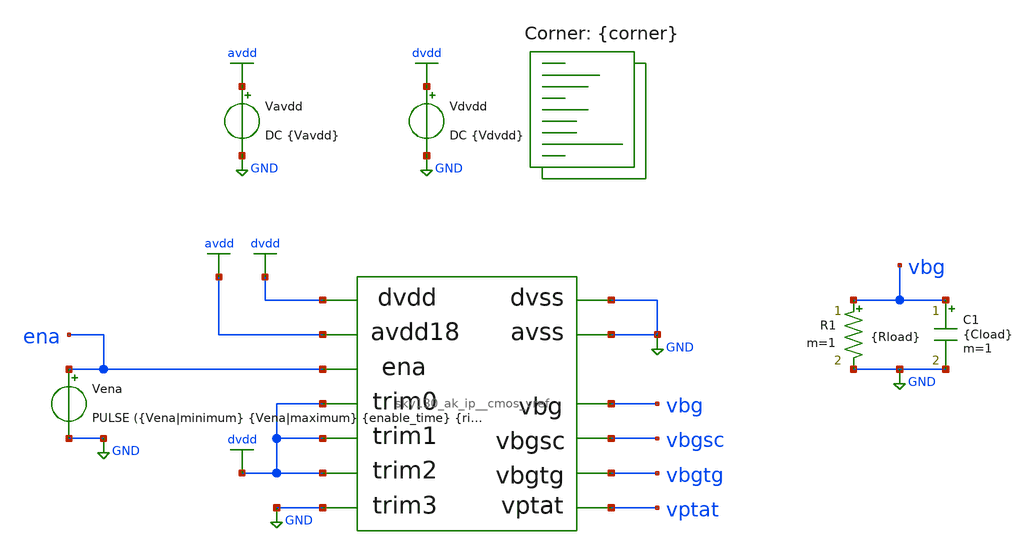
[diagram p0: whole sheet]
** sch_path: cace/tb_startup.sch
**.subckt tb_startup
Vavdd avdd GND DC {Vavdd}
X1 avdd GND dvdd vbg vptat dvdd dvdd GND dvdd GND ena vbgsc vbgtg sky130_ak_ip__cmos_vref
Vdvdd dvdd GND DC {Vdvdd}
C1 vbg GND {Cload} m=1
Vena ena GND PULSE ({Vena|minimum} {Vena|maximum} {enable_time} {rise_time})
R1 vbg GND {Rload} m=1
**** begin user architecture code


.option TEMP={temperature}
.option warn=1
.control
save vbg, ena
tran {tran_step} {tran_stop} {tran_start}
let vref_data = V(vbg)
wrdata {simpath}/{filename}_{N}.data V(vbg)
quit
.endc


.lib $::SKYWATER_MODELS/sky130.lib.spice {corner}
 .include $::SKYWATER_STDCELLS/sky130_fd_sc_hd.spice
**** end user architecture code
**.ends
.GLOBAL avdd
.GLOBAL GND
.GLOBAL dvdd
.end
